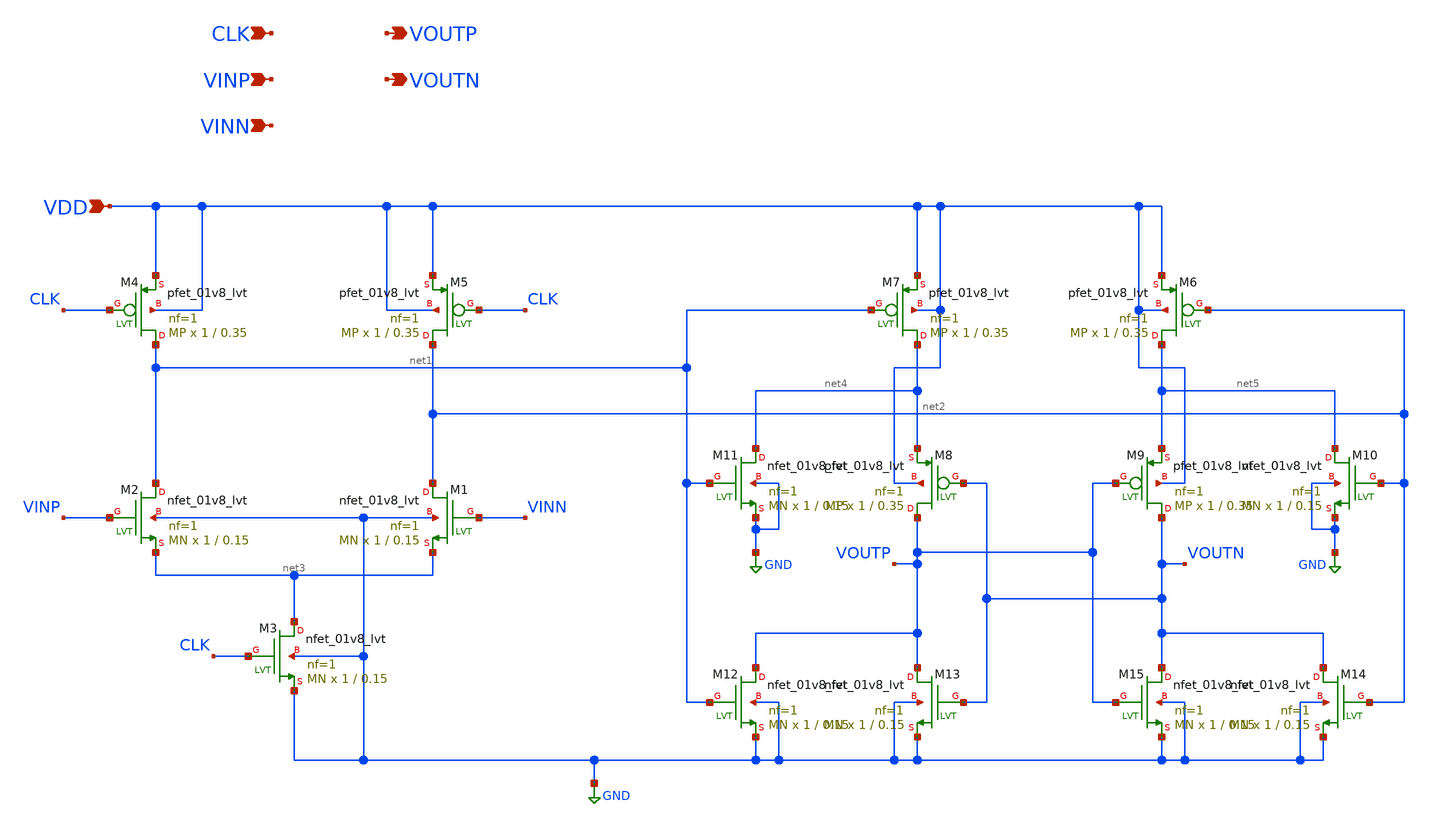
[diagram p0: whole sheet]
** sch_path: xschem/my_comparator.sch
**.subckt my_comparator VDD VOUTN VOUTP CLK VINP VINN
*.ipin VDD
*.opin VOUTN
*.opin VOUTP
*.ipin CLK
*.ipin VINP
*.ipin VINN
XM2 net1 VINP net3 GND sky130_fd_pr__nfet_01v8_lvt L=0.15 W=1 nf=1 ad='int((nf+1)/2) * W/nf * 0.29' as='int((nf+2)/2) * W/nf * 0.29'
+ pd='2*int((nf+1)/2) * (W/nf + 0.29)' ps='2*int((nf+2)/2) * (W/nf + 0.29)' nrd='0.29 / W' nrs='0.29 / W'
+ sa=0 sb=0 sd=0 mult=MN m=MN
XM4 net1 CLK VDD VDD sky130_fd_pr__pfet_01v8_lvt L=0.35 W=1 nf=1 ad='int((nf+1)/2) * W/nf * 0.29' as='int((nf+2)/2) * W/nf * 0.29'
+ pd='2*int((nf+1)/2) * (W/nf + 0.29)' ps='2*int((nf+2)/2) * (W/nf + 0.29)' nrd='0.29 / W' nrs='0.29 / W'
+ sa=0 sb=0 sd=0 mult=MP m=MP
XM5 net2 CLK VDD VDD sky130_fd_pr__pfet_01v8_lvt L=0.35 W=1 nf=1 ad='int((nf+1)/2) * W/nf * 0.29' as='int((nf+2)/2) * W/nf * 0.29'
+ pd='2*int((nf+1)/2) * (W/nf + 0.29)' ps='2*int((nf+2)/2) * (W/nf + 0.29)' nrd='0.29 / W' nrs='0.29 / W'
+ sa=0 sb=0 sd=0 mult=MP m=MP
XM6 net5 net2 VDD VDD sky130_fd_pr__pfet_01v8_lvt L=0.35 W=1 nf=1 ad='int((nf+1)/2) * W/nf * 0.29' as='int((nf+2)/2) * W/nf * 0.29'
+ pd='2*int((nf+1)/2) * (W/nf + 0.29)' ps='2*int((nf+2)/2) * (W/nf + 0.29)' nrd='0.29 / W' nrs='0.29 / W'
+ sa=0 sb=0 sd=0 mult=MP m=MP
XM7 net4 net1 VDD VDD sky130_fd_pr__pfet_01v8_lvt L=0.35 W=1 nf=1 ad='int((nf+1)/2) * W/nf * 0.29' as='int((nf+2)/2) * W/nf * 0.29'
+ pd='2*int((nf+1)/2) * (W/nf + 0.29)' ps='2*int((nf+2)/2) * (W/nf + 0.29)' nrd='0.29 / W' nrs='0.29 / W'
+ sa=0 sb=0 sd=0 mult=MP m=MP
XM8 VOUTP VOUTN net4 VDD sky130_fd_pr__pfet_01v8_lvt L=0.35 W=1 nf=1 ad='int((nf+1)/2) * W/nf * 0.29'
+ as='int((nf+2)/2) * W/nf * 0.29' pd='2*int((nf+1)/2) * (W/nf + 0.29)' ps='2*int((nf+2)/2) * (W/nf + 0.29)'
+ nrd='0.29 / W' nrs='0.29 / W' sa=0 sb=0 sd=0 mult=MP m=MP
XM9 VOUTN VOUTP net5 VDD sky130_fd_pr__pfet_01v8_lvt L=0.35 W=1 nf=1 ad='int((nf+1)/2) * W/nf * 0.29'
+ as='int((nf+2)/2) * W/nf * 0.29' pd='2*int((nf+1)/2) * (W/nf + 0.29)' ps='2*int((nf+2)/2) * (W/nf + 0.29)'
+ nrd='0.29 / W' nrs='0.29 / W' sa=0 sb=0 sd=0 mult=MP m=MP
XM1 net2 VINN net3 GND sky130_fd_pr__nfet_01v8_lvt L=0.15 W=1 nf=1 ad='int((nf+1)/2) * W/nf * 0.29' as='int((nf+2)/2) * W/nf * 0.29'
+ pd='2*int((nf+1)/2) * (W/nf + 0.29)' ps='2*int((nf+2)/2) * (W/nf + 0.29)' nrd='0.29 / W' nrs='0.29 / W'
+ sa=0 sb=0 sd=0 mult=MN m=MN
XM3 net3 CLK GND GND sky130_fd_pr__nfet_01v8_lvt L=0.15 W=1 nf=1 ad='int((nf+1)/2) * W/nf * 0.29' as='int((nf+2)/2) * W/nf * 0.29'
+ pd='2*int((nf+1)/2) * (W/nf + 0.29)' ps='2*int((nf+2)/2) * (W/nf + 0.29)' nrd='0.29 / W' nrs='0.29 / W'
+ sa=0 sb=0 sd=0 mult=MN m=MN
XM10 net5 net2 GND GND sky130_fd_pr__nfet_01v8_lvt L=0.15 W=1 nf=1 ad='int((nf+1)/2) * W/nf * 0.29' as='int((nf+2)/2) * W/nf * 0.29'
+ pd='2*int((nf+1)/2) * (W/nf + 0.29)' ps='2*int((nf+2)/2) * (W/nf + 0.29)' nrd='0.29 / W' nrs='0.29 / W'
+ sa=0 sb=0 sd=0 mult=MN m=MN
XM11 net4 net1 GND GND sky130_fd_pr__nfet_01v8_lvt L=0.15 W=1 nf=1 ad='int((nf+1)/2) * W/nf * 0.29' as='int((nf+2)/2) * W/nf * 0.29'
+ pd='2*int((nf+1)/2) * (W/nf + 0.29)' ps='2*int((nf+2)/2) * (W/nf + 0.29)' nrd='0.29 / W' nrs='0.29 / W'
+ sa=0 sb=0 sd=0 mult=MN m=MN
XM12 VOUTP net1 GND GND sky130_fd_pr__nfet_01v8_lvt L=0.15 W=1 nf=1 ad='int((nf+1)/2) * W/nf * 0.29'
+ as='int((nf+2)/2) * W/nf * 0.29' pd='2*int((nf+1)/2) * (W/nf + 0.29)' ps='2*int((nf+2)/2) * (W/nf + 0.29)'
+ nrd='0.29 / W' nrs='0.29 / W' sa=0 sb=0 sd=0 mult=MN m=MN
XM13 VOUTP VOUTN GND GND sky130_fd_pr__nfet_01v8_lvt L=0.15 W=1 nf=1 ad='int((nf+1)/2) * W/nf * 0.29'
+ as='int((nf+2)/2) * W/nf * 0.29' pd='2*int((nf+1)/2) * (W/nf + 0.29)' ps='2*int((nf+2)/2) * (W/nf + 0.29)'
+ nrd='0.29 / W' nrs='0.29 / W' sa=0 sb=0 sd=0 mult=MN m=MN
XM14 VOUTN net2 GND GND sky130_fd_pr__nfet_01v8_lvt L=0.15 W=1 nf=1 ad='int((nf+1)/2) * W/nf * 0.29'
+ as='int((nf+2)/2) * W/nf * 0.29' pd='2*int((nf+1)/2) * (W/nf + 0.29)' ps='2*int((nf+2)/2) * (W/nf + 0.29)'
+ nrd='0.29 / W' nrs='0.29 / W' sa=0 sb=0 sd=0 mult=MN m=MN
XM15 VOUTN VOUTP GND GND sky130_fd_pr__nfet_01v8_lvt L=0.15 W=1 nf=1 ad='int((nf+1)/2) * W/nf * 0.29'
+ as='int((nf+2)/2) * W/nf * 0.29' pd='2*int((nf+1)/2) * (W/nf + 0.29)' ps='2*int((nf+2)/2) * (W/nf + 0.29)'
+ nrd='0.29 / W' nrs='0.29 / W' sa=0 sb=0 sd=0 mult=MN m=MN
**** begin user architecture code


.param MP=1
.param MN=1


**** end user architecture code
**.ends
.GLOBAL GND
.end
